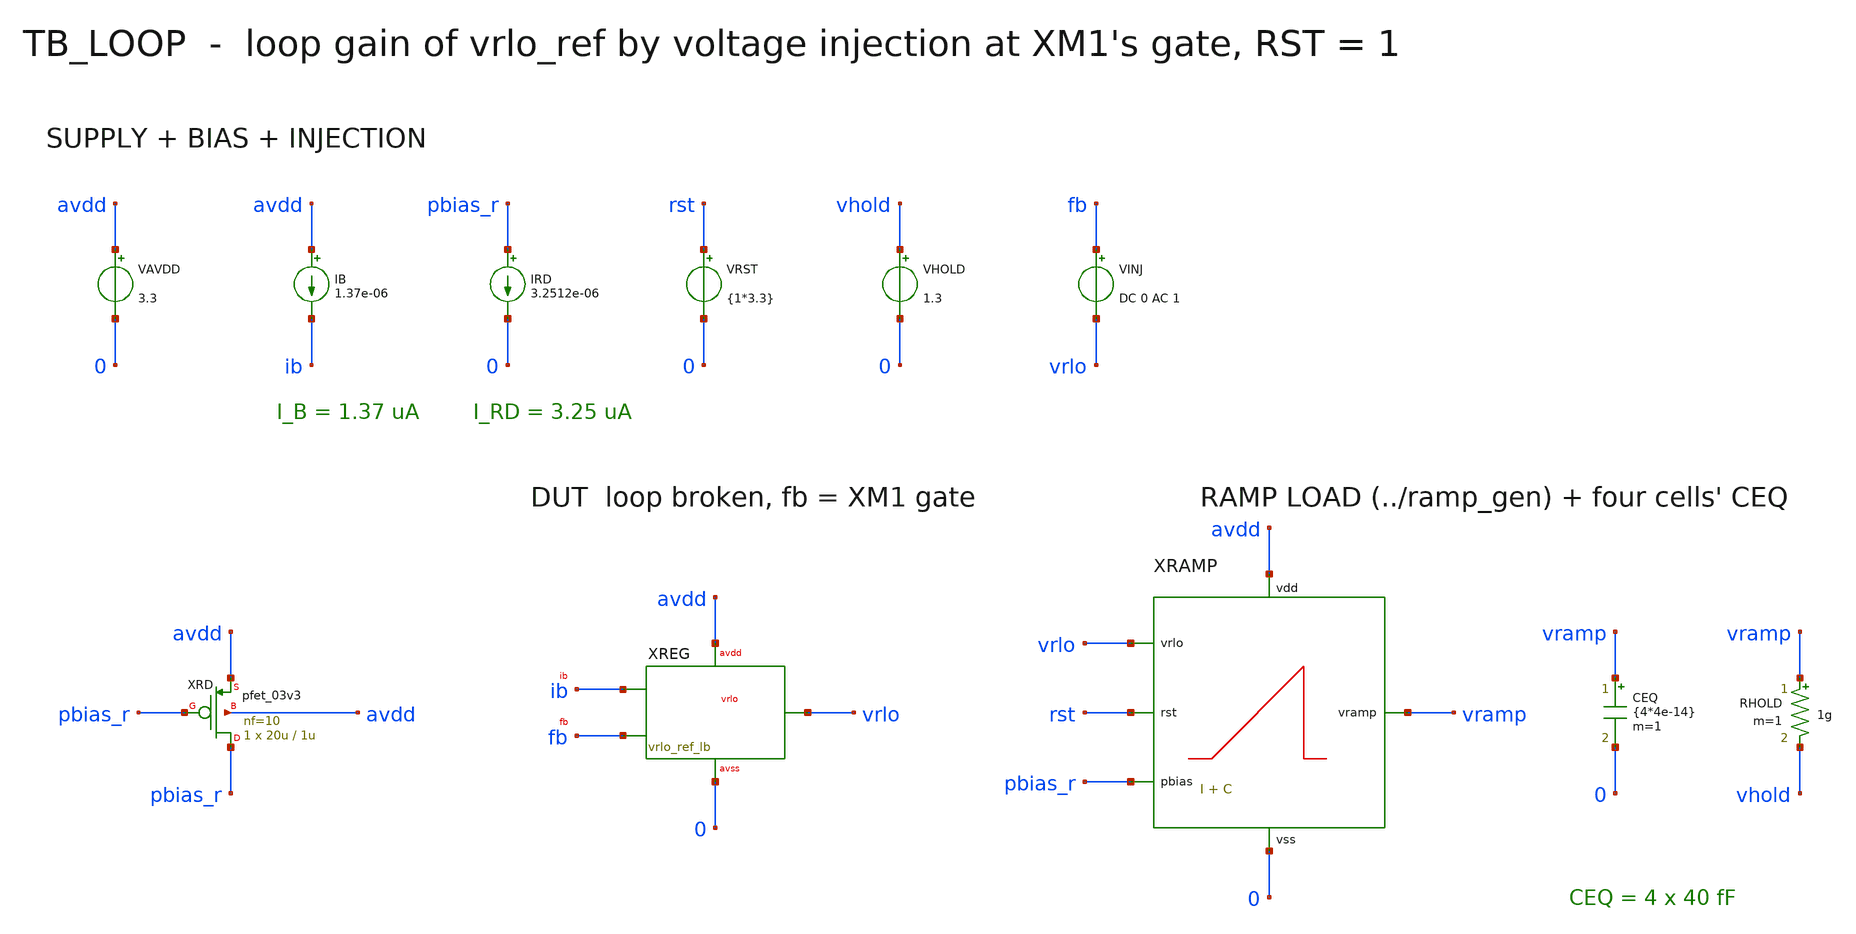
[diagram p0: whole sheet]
** sch_path: mixed_signal/vrlo_ref/tb_loop.sch
**.subckt tb_loop
VAVDD avdd 0 3.3
IB avdd ib 1.37e-06
XREG vrlo fb ib avdd 0 vrlo_ref_lb
VINJ fb vrlo DC 0 AC 1
IRD pbias_r 0 3.2512e-06
XRD pbias_r pbias_r avdd avdd pfet_03v3 L=1u W=20u nf=10 m=1
VRST rst 0 {1*3.3}
XRAMP vramp rst vrlo pbias_r avdd 0 ramp_simple
CEQ vramp 0 {4*4e-14} m=1
RHOLD vramp vhold 1g m=1
VHOLD vhold 0 1.3
**** begin user architecture code

.include /foss/pdks/gf180mcuD/libs.tech/ngspice/design.ngspice
.lib /foss/pdks/gf180mcuD/libs.tech/ngspice/sm141064.ngspice typical
.lib /foss/pdks/gf180mcuD/libs.tech/ngspice/sm141064.ngspice res_typical
.lib /foss/pdks/gf180mcuD/libs.tech/ngspice/sm141064.ngspice mimcap_typical
.include /foss/designs/mixed_signal/ramp_gen/data/ramp_simple_params.spice
.include /foss/designs/mixed_signal/vrlo_ref/work/dut_lb.spice
.temp 27
.options gmin=1e-15
.control
set num_threads=1
op
ac dec 40 10 10g
let t = -v(vrlo)/v(fb)
let tdb = db(t)
let tph = 180/pi*cph(t)
meas ac ugb_hz WHEN tdb=0 FALL=1
meas ac ph_ugb FIND tph AT=ugb_hz
let pm = 180 + ph_ugb
let pmr = pm - 360*floor((pm+180)/360)
echo pm_deg = $&pmr
meas ac t0_db FIND tdb AT=10
quit
.endc

**** end user architecture code
**.ends
.end
